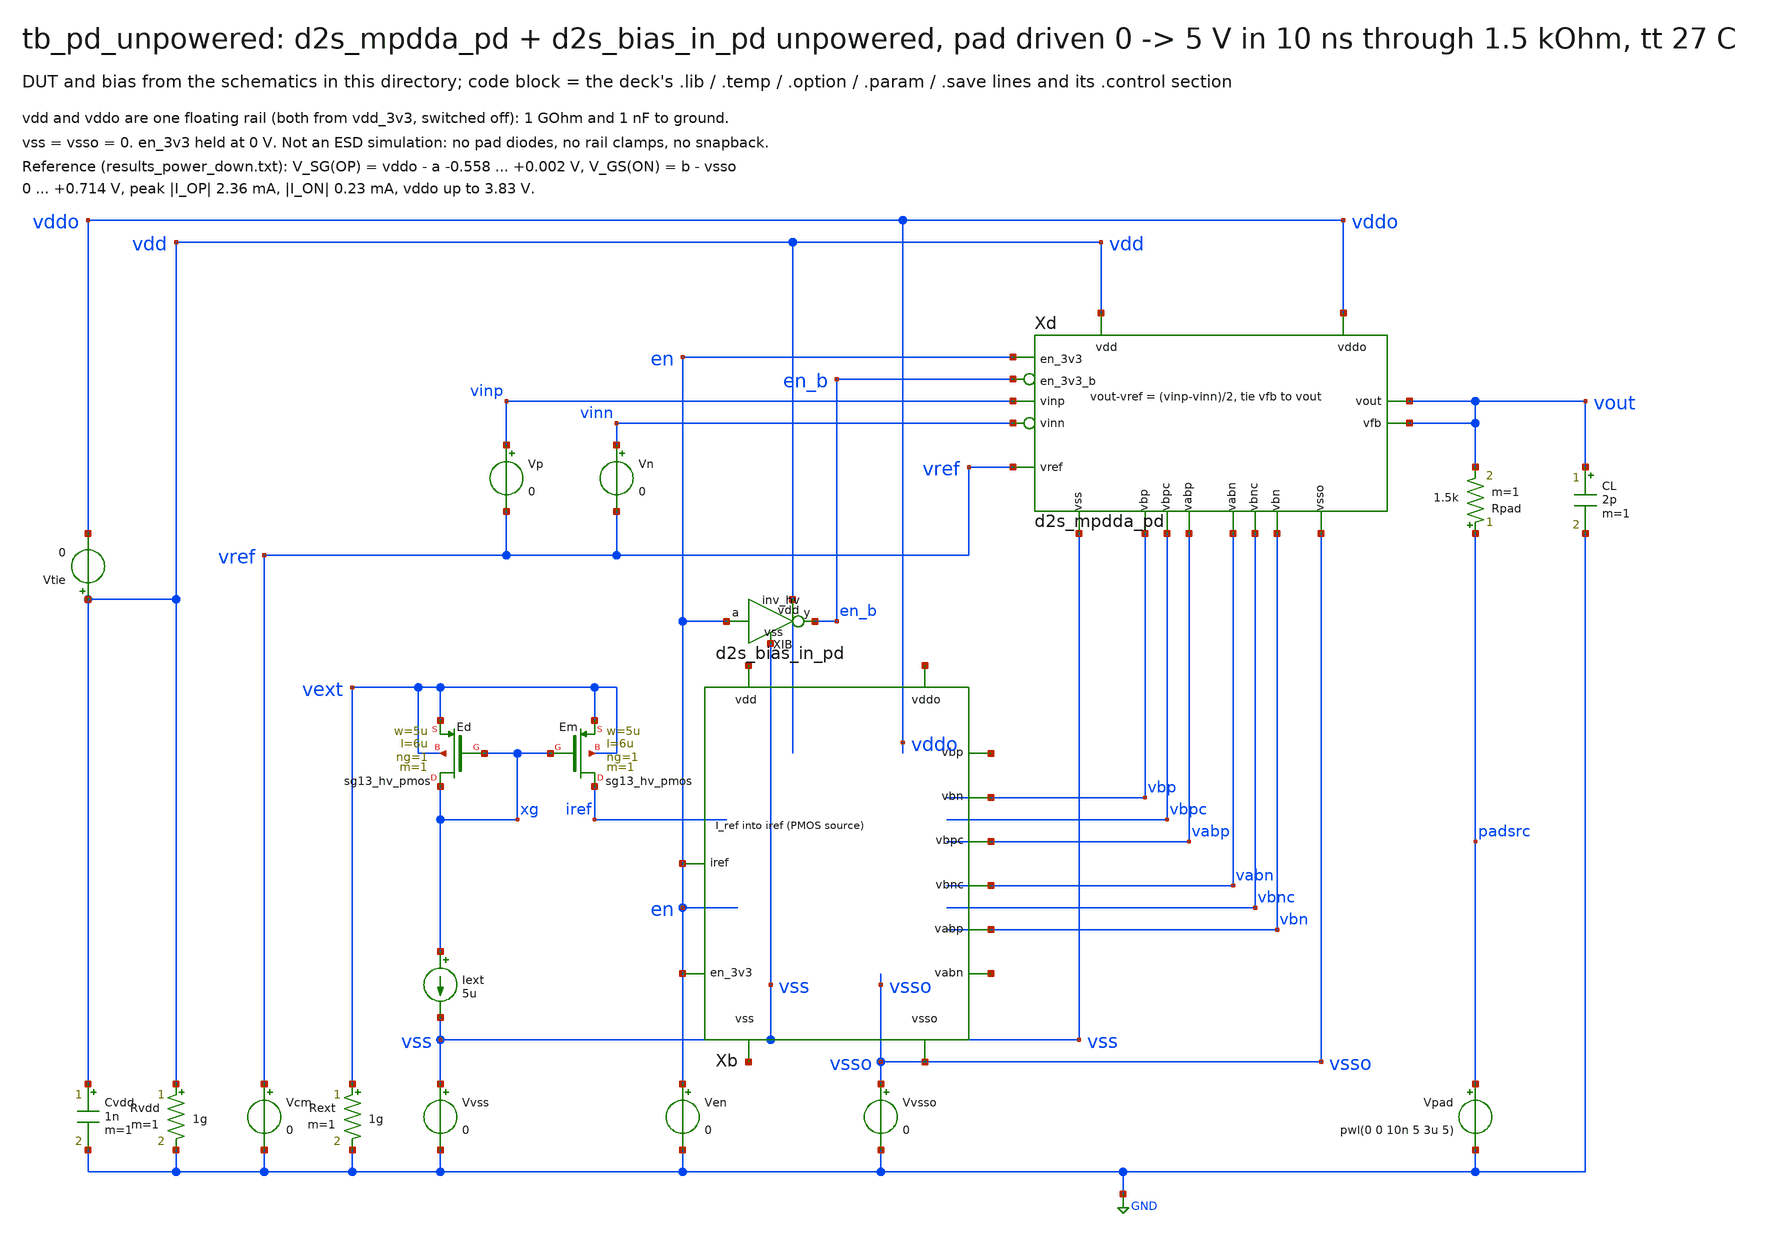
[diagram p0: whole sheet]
** sch_path: sudelbuecher/design_considerations/consolidation/bias_hierarchy_2026-10-27/before/macros/sg13cmos5l_IOPadDiff2Single/testbenches/xschem/tb_pd_unpowered.sch
**.subckt tb_pd_unpowered
Vvss vss GND 0
Vvsso vsso GND 0
Ven en GND 0
Vcm vref GND 0
Xb net1 net2 net3 vsso en net4 vbp vabp vabn vbn net5 en d2s_bias_in_pd
Xd vdd vss vddo vsso vinp vinn vref vout vout vbp vbn vbpc vbnc vabp vabn en en_b d2s_mpdda_pd
Vp vinp vref 0
Vn vinn vref 0
XEd xg xg vext vext sg13_hv_pmos w=5u l=6u ng=1 m=1 mm_ok=1
XEm iref xg vext vext sg13_hv_pmos w=5u l=6u ng=1 m=1 mm_ok=1
Iext xg vss 5u
CL vout GND 2p m=1
Rvdd vdd GND 1g m=1
Cvdd vdd GND 1n m=1
Vtie vdd vddo 0
Rext vext GND 1g m=1
Rpad padsrc vout 1.5k m=1
Vpad padsrc GND pwl(0 0 10n 5 3u 5)
XIB vdd vss en en_b inv_hv
**** begin user architecture code

.lib cornerMOShv.lib mos_tt
.lib cornerRES.lib res_typ
.lib cornerCAP.lib cap_typ
.temp 27
.option method=gear
.save v(vout) v(xd.a) v(xd.b) v(vddo) v(en_b) @n.xd.xop.nsg13_hv_pmos[ids] @n.xd.xon.nsg13_hv_nmos[ids]
.control
tran 1n 3u uic
let vsg_op = v(vddo) - v(xd.a)
let vgs_on = v(xd.b)
meas tran pmin min vsg_op
meas tran pmax max vsg_op
meas tran nmin min vgs_on
meas tran nmax max vgs_on
let ip = abs(@n.xd.xop.nsg13_hv_pmos[ids])
let inn = abs(@n.xd.xon.nsg13_hv_nmos[ids])
meas tran ipm max ip
meas tran inm max inn
meas tran vddm max v(vddo)
print pmin pmax nmin nmax ipm inm vddm
if $?batchmode = 0
  plot v(vout) v(vddo) v(xd.a) v(xd.b) v(en_b)
end
.endc

**** end user architecture code
**.ends
.GLOBAL GND
.end
